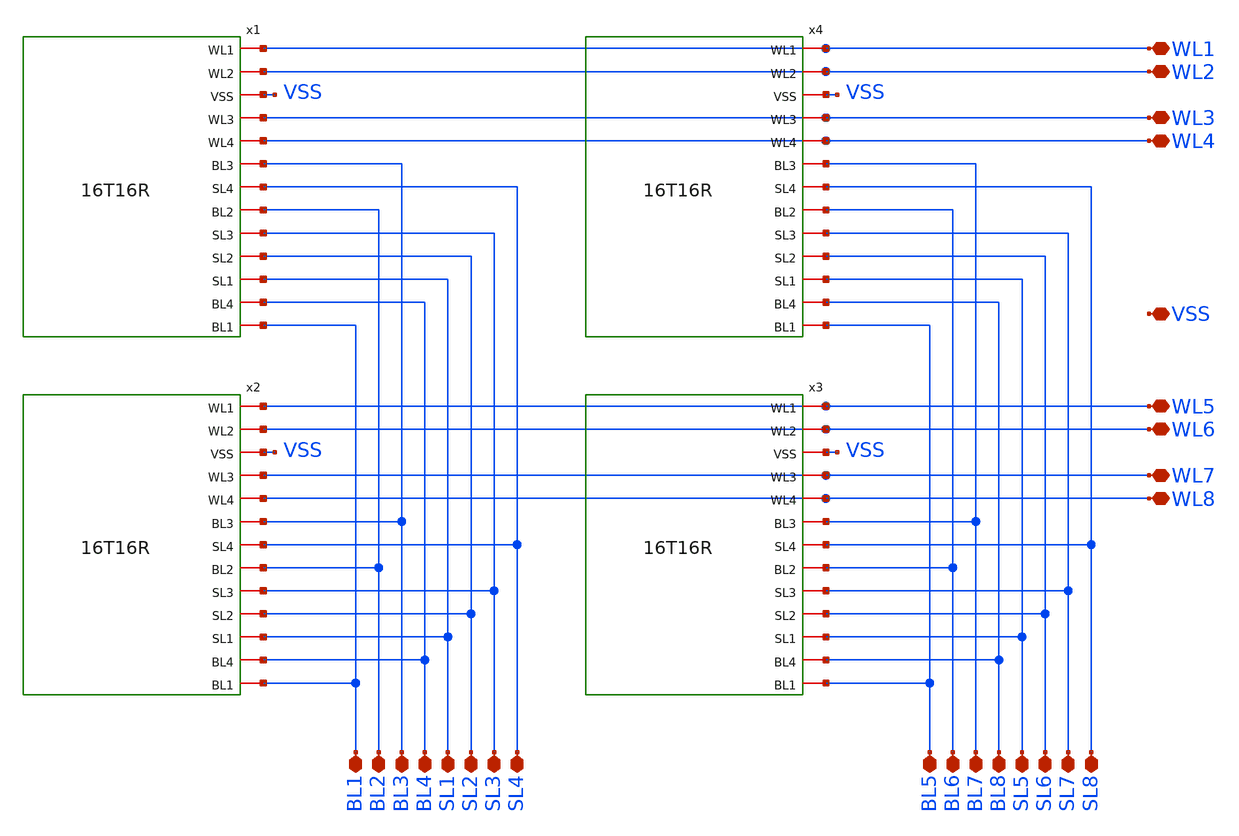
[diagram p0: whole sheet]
** sch_path: xschem/64T64R.sch
* StefanSchippers/xschem_sky130/sky130_fd_pr/reram.sym:
* Copyright 2021 Stefan Frederik Schippers
* Licensed under the Apache License, Version 2.0 (the "License");
**.subckt 64T64R VSS WL1 WL2 WL3 WL4 WL5 WL6 WL7 WL8 BL1 BL2 BL3 BL4 BL5 BL6 BL7 BL8 SL1 SL2 SL3 SL4
*+ SL5 SL6 SL7 SL8
*.iopin VSS
*.iopin WL1
*.iopin WL2
*.iopin WL3
*.iopin WL4
*.iopin WL5
*.iopin WL6
*.iopin WL7
*.iopin WL8
*.iopin BL1
*.iopin BL2
*.iopin BL3
*.iopin BL4
*.iopin BL5
*.iopin BL6
*.iopin BL7
*.iopin BL8
*.iopin SL1
*.iopin SL2
*.iopin SL3
*.iopin SL4
*.iopin SL5
*.iopin SL6
*.iopin SL7
*.iopin SL8
x1 WL1 WL2 VSS WL3 WL4 BL3 SL4 BL2 SL3 SL2 SL1 BL4 BL1 16T16R
x2 WL5 WL6 VSS WL7 WL8 BL3 SL4 BL2 SL3 SL2 SL1 BL4 BL1 16T16R
x3 WL5 WL6 VSS WL7 WL8 BL7 SL8 BL6 SL7 SL6 SL5 BL8 BL5 16T16R
x4 WL1 WL2 VSS WL3 WL4 BL7 SL8 BL6 SL7 SL6 SL5 BL8 BL5 16T16R
**.ends

* expanding   symbol:  16T16R.sym # of pins=13
** sym_path: xschem/16T16R.sym
** sch_path: xschem/16T16R.sch
.subckt 16T16R WL1 WL2 VSS WL3 WL4 BL3 SL4 BL2 SL3 SL2 SL1 BL4 BL1
*.iopin WL1
*.iopin WL2
*.iopin WL3
*.iopin WL4
*.iopin BL1
*.iopin BL2
*.iopin BL3
*.iopin BL4
*.iopin SL1
*.iopin SL2
*.iopin SL3
*.iopin SL4
*.iopin VSS
x1 WL1 VSS WL2 BL2 SL1 SL2 BL1 4T4R
x2 WL3 VSS WL4 BL2 SL1 SL2 BL1 4T4R
x3 WL1 VSS WL2 BL4 SL3 SL4 BL3 4T4R
x4 WL3 VSS WL4 BL4 SL3 SL4 BL3 4T4R
.ends


* expanding   symbol:  4T4R.sym # of pins=7
** sym_path: xschem/4T4R.sym
** sch_path: xschem/4T4R.sch
.subckt 4T4R WL1 VSS WL2 BL2 SL1 SL2 BL1
*.iopin VSS
*.iopin BL1
*.iopin BL2
*.iopin WL1
*.iopin WL2
*.iopin SL1
*.iopin SL2
x1 BL1 WL1 VSS SL1 1T1R
x2 BL1 WL2 VSS SL1 1T1R
x3 BL2 WL1 VSS SL2 1T1R
x4 BL2 WL2 VSS SL2 1T1R
.ends


* expanding   symbol:  1T1R.sym # of pins=4
** sym_path: xschem/1T1R.sym
** sch_path: xschem/1T1R.sch
.subckt 1T1R BL WL VSS SL
*.iopin SL
*.iopin VSS
*.iopin WL
*.iopin BL
XR1 BL net1 sky130_fd_pr_reram__reram_cell Tfilament_0=3.8e-9
XM1 net1 WL SL VSS sky130_fd_pr__nfet_g5v0d10v5 L=0.5 W=7 nf=1 ad='int((nf+1)/2) * W/nf * 0.29' as='int((nf+2)/2) * W/nf * 0.29'
+ pd='2*int((nf+1)/2) * (W/nf + 0.29)' ps='2*int((nf+2)/2) * (W/nf + 0.29)' nrd='0.29 / W' nrs='0.29 / W'
+ sa=0 sb=0 sd=0 mult=1 m=1
.ends

**** begin user architecture code

.subckt sky130_fd_pr_reram__reram_cell TE BE Tfilament_0=3.3e-9 area_ox=0.1024e-12
N1 TE BE nFilament sky130_fd_pr_reram__reram_model
.ic v(nFilament)={Tfilament_0*1.0e9}
.ends sky130_fd_pr_reram__reram_cell

.model sky130_fd_pr_reram__reram_model sky130_fd_pr_reram__reram_module  area_ox = 0.1024e-12  Tox =
+ 5.0  Tfilament_max = 4.9  Tfilament_min = 3.3  Eact_generation = 1.501  Eact_recombination  = 1.500
+  I_k1  = 6.140e-5  Tfilament_ref = 4.7249  V_ref = 0.430  velocity_k1 = 150  gamma_k0  = 16.5  gamma_k1
+  = -1.25  Temperature_0 = 300  C_thermal = 3.1825e-16  tau_thermal = 0.23e-9  t_step  = 1.0e-9
+  smoothing = 1e-7  Kclip = 200

.control
pre_osdi $SKYWATER_MODELS/sky130_fd_pr_reram__reram_module.osdi
.endc

**** end user architecture code
.end
